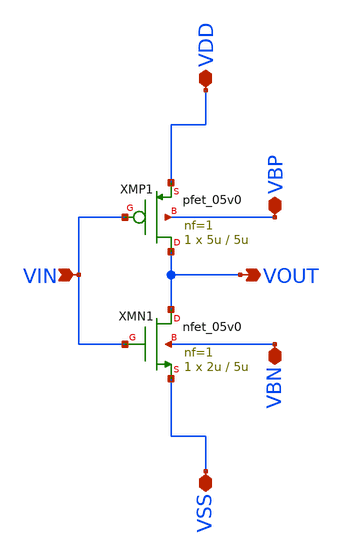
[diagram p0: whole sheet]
** sch_path: xschem/vco/vco_inv_forlvs.sch
**.subckt vco_inv_forlvs VDD VSS VIN VOUT VBP VBN
*.iopin VDD
*.iopin VSS
*.ipin VIN
*.opin VOUT
*.iopin VBP
*.iopin VBN
XMN1 VOUT VIN VSS VBN nfet_05v0 L=5u W=2u nf=1 ad='int((nf+1)/2) * W/nf * 0.18u' as='int((nf+2)/2) * W/nf * 0.18u'
+ pd='2*int((nf+1)/2) * (W/nf + 0.18u)' ps='2*int((nf+2)/2) * (W/nf + 0.18u)' nrd='0.18u / W' nrs='0.18u / W'
+ sa=0 sb=0 sd=0 m=1
XMP1 VOUT VIN VDD VBP pfet_05v0 L=5u W=5u nf=1 ad='int((nf+1)/2) * W/nf * 0.18u' as='int((nf+2)/2) * W/nf * 0.18u'
+ pd='2*int((nf+1)/2) * (W/nf + 0.18u)' ps='2*int((nf+2)/2) * (W/nf + 0.18u)' nrd='0.18u / W' nrs='0.18u / W'
+ sa=0 sb=0 sd=0 m=1
**.ends
.end
